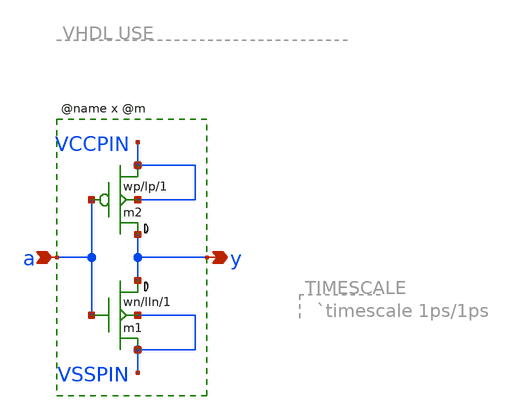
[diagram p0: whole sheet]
** sch_path: xschem_library/rom8k/lvnot.sch
**.subckt lvnot y a
*.opin y
*.ipin a
m2 y a VCCPIN VCCPIN cmosp w=wp l=lp ad='wp *4.6u' as='wp *4.6u' pd='wp *2+9.2u' ps='wp *2+9.2u' m=1
m1 y a VSSPIN VSSPIN cmosn w=wn l=lln ad='wn *4.3u' as='wn *4.3u' pd='wn *2+8.6u' ps='wn *2+8.6u' m=1
**.ends
.end
